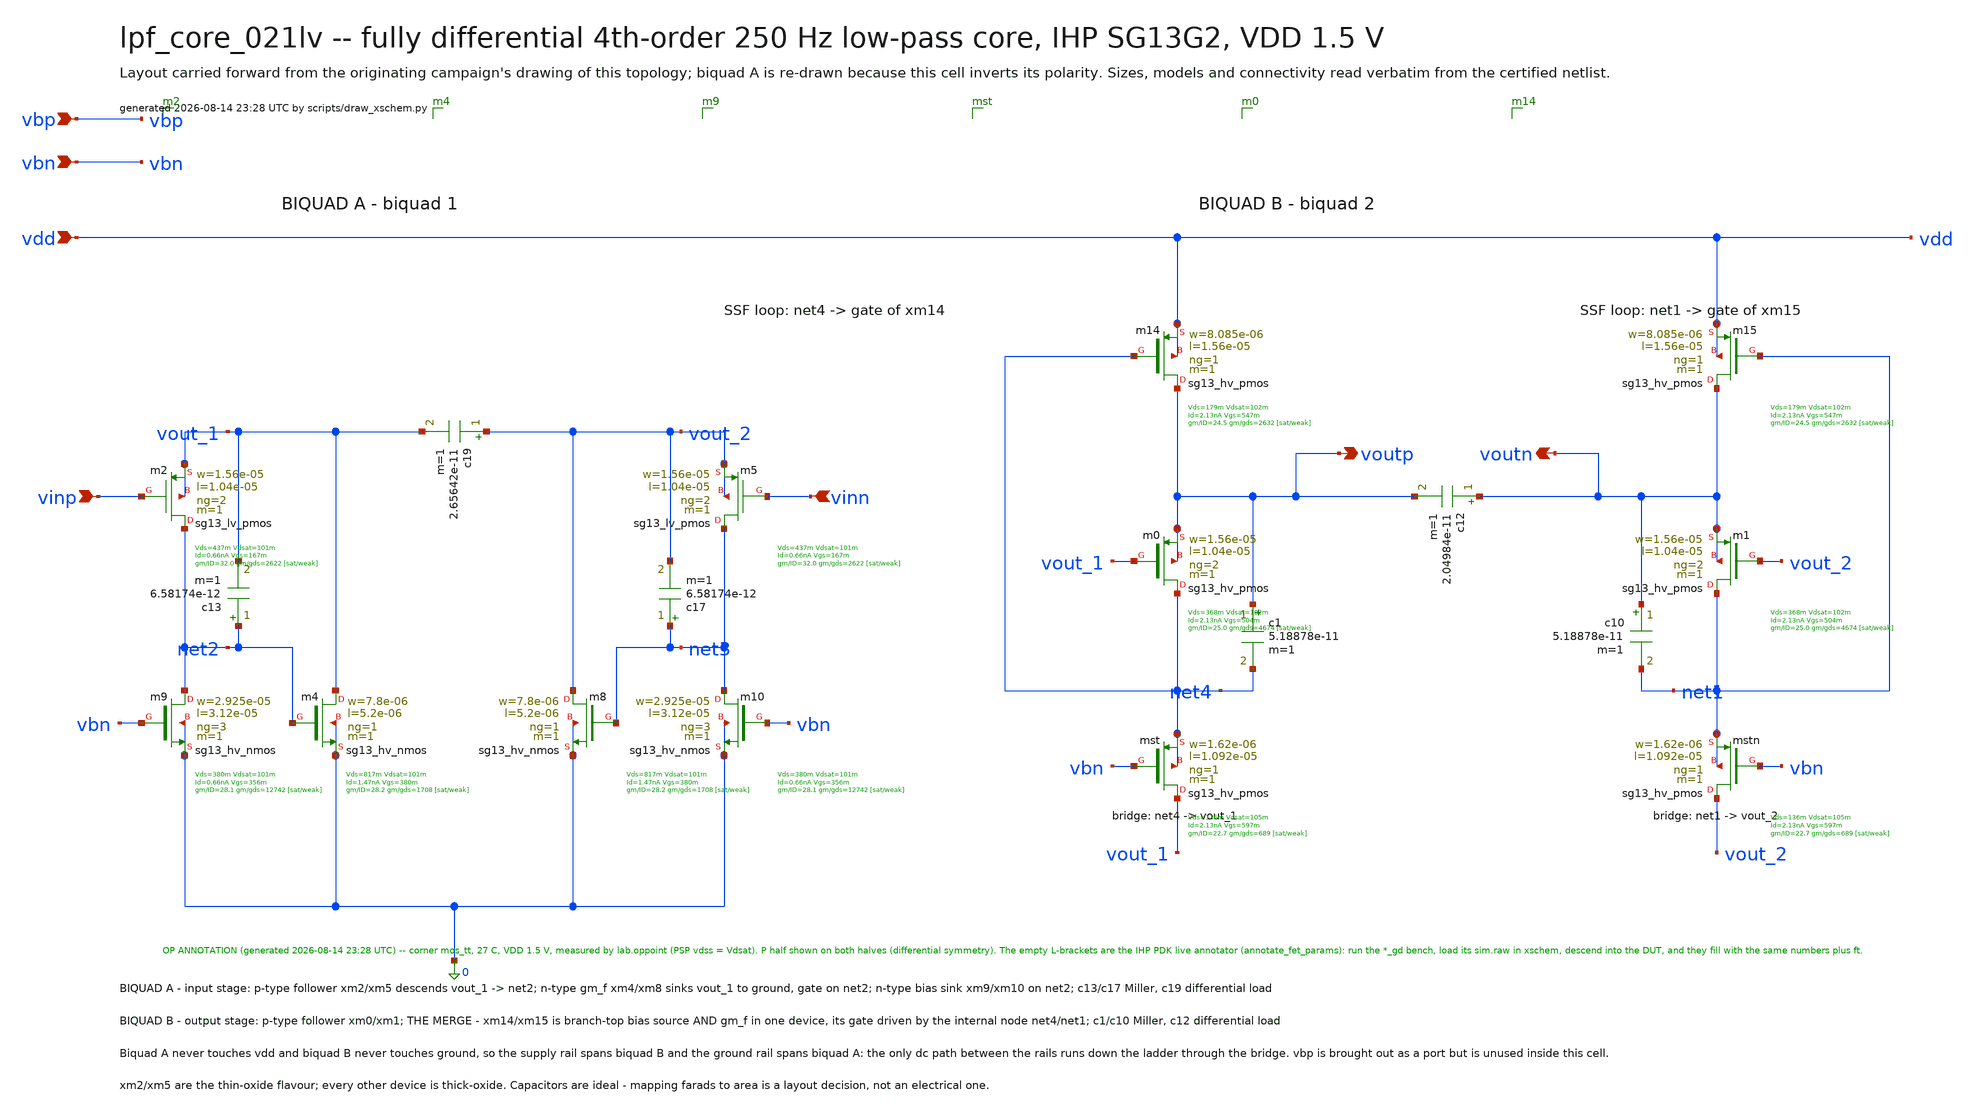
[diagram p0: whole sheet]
** sch_path: signoff/pre-pvt/schematic/lpf_core_021lv.sch
**.subckt lpf_core_021lv vinp vinn voutp voutn vdd vbn vbp
*.ipin vinp
*.ipin vinn
*.opin voutp
*.opin voutn
*.ipin vdd
*.ipin vbn
*.ipin vbp
Xm2 net2 vinp vout_1 vout_1 sg13_lv_pmos w=1.56e-05 l=1.04e-05 ng=2 m=1 mm_ok=1
Xm5 net3 vinn vout_2 vout_2 sg13_lv_pmos w=1.56e-05 l=1.04e-05 ng=2 m=1 mm_ok=1
Xm4 vout_1 net2 0 0 sg13_hv_nmos w=7.8e-06 l=5.2e-06 ng=1 m=1 mm_ok=1
Xm8 vout_2 net3 0 0 sg13_hv_nmos w=7.8e-06 l=5.2e-06 ng=1 m=1 mm_ok=1
Xm9 net2 vbn 0 0 sg13_hv_nmos w=2.925e-05 l=3.12e-05 ng=3 m=1 mm_ok=1
Xm10 net3 vbn 0 0 sg13_hv_nmos w=2.925e-05 l=3.12e-05 ng=3 m=1 mm_ok=1
Xmst vout_1 vbn net4 net4 sg13_hv_pmos w=1.62e-06 l=1.092e-05 ng=1 m=1 mm_ok=1
Xmstn vout_2 vbn net1 net1 sg13_hv_pmos w=1.62e-06 l=1.092e-05 ng=1 m=1 mm_ok=1
Xm0 net4 vout_1 voutp voutp sg13_hv_pmos w=1.56e-05 l=1.04e-05 ng=2 m=1 mm_ok=1
Xm1 net1 vout_2 voutn voutn sg13_hv_pmos w=1.56e-05 l=1.04e-05 ng=2 m=1 mm_ok=1
Xm14 voutp net4 vdd vdd sg13_hv_pmos w=8.085e-06 l=1.56e-05 ng=1 m=1 mm_ok=1
Xm15 voutn net1 vdd vdd sg13_hv_pmos w=8.085e-06 l=1.56e-05 ng=1 m=1 mm_ok=1
c13 net2 vout_1 6.58174e-12 m=1
c17 net3 vout_2 6.58174e-12 m=1
c19 vout_2 vout_1 2.65642e-11 m=1
c1 voutp net4 5.18878e-11 m=1
c10 voutn net1 5.18878e-11 m=1
c12 voutn voutp 2.04984e-11 m=1
**.ends
.end
